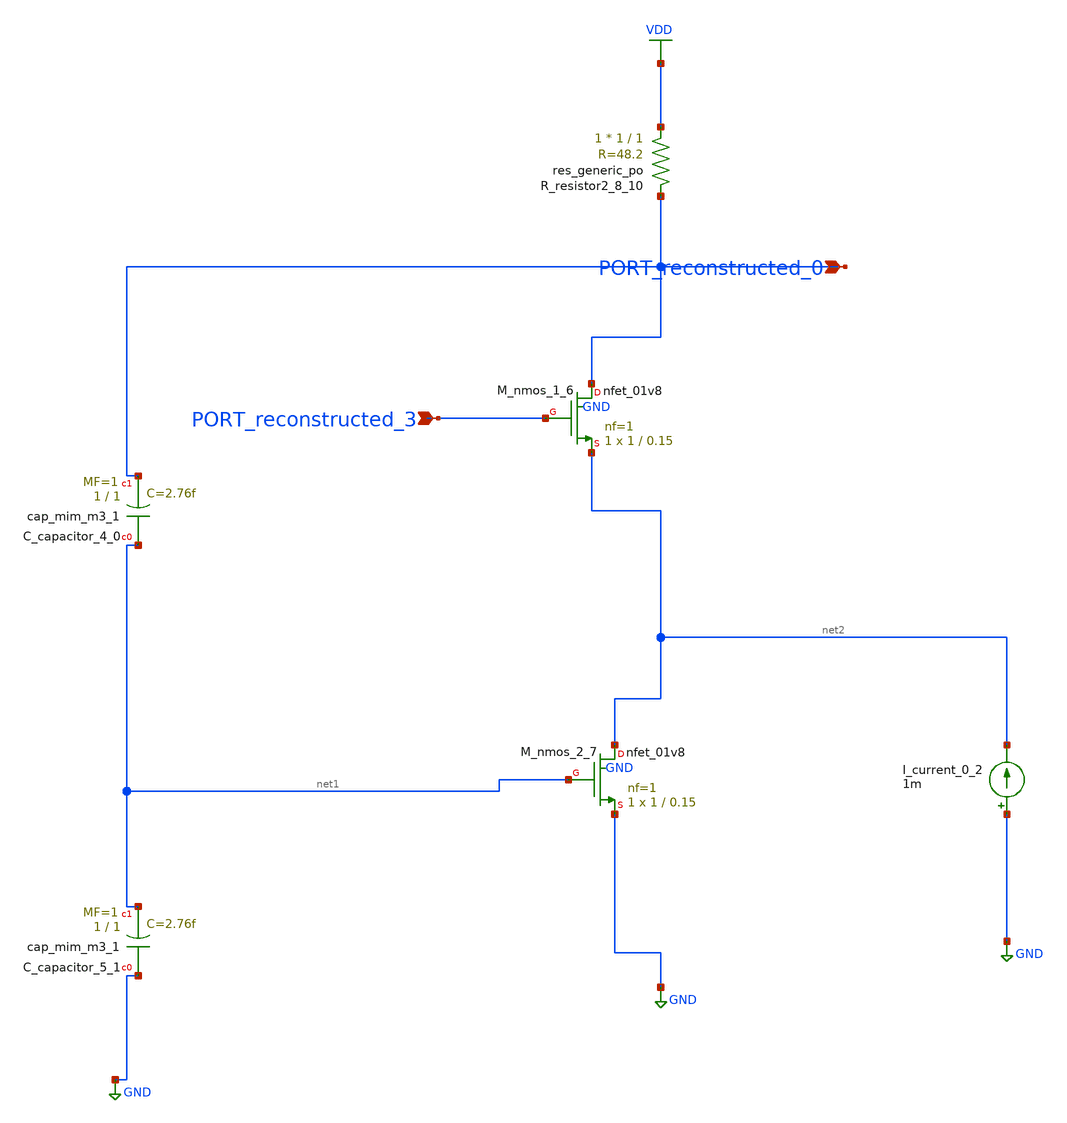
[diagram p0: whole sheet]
** sch_path: schematics/AMSNet/558.sch
**.subckt 558 PORT_reconstructed_0 PORT_reconstructed_3
*.ipin PORT_reconstructed_0
*.ipin PORT_reconstructed_3
XC_capacitor_4_0 net1 PORT_reconstructed_0 sky130_fd_pr__cap_mim_m3_1 W=1 L=1 MF=1 m=1
XC_capacitor_5_1 GND net1 sky130_fd_pr__cap_mim_m3_1 W=1 L=1 MF=1 m=1
I_current_0_2 GND net2 1m
XM_nmos_1_6 PORT_reconstructed_0 PORT_reconstructed_3 net2 GND sky130_fd_pr__nfet_01v8 L=0.15 W=1 nf=1
+ ad='int((1 + 1)/2) * 1 / 1 * 0.29' as='int((1 + 2)/2) * 1 / 1 * 0.29' pd='2*int((1 + 1)/2) * (1 / 1 + 0.29)'
+ ps='2*int((1 + 2)/2) * (1 / 1 + 0.29)' nrd='0.29 / 1 ' nrs='0.29 / 1 ' sa=0 sb=0 sd=0 mult=1 m=1
XM_nmos_2_7 net2 net1 GND GND sky130_fd_pr__nfet_01v8 L=0.15 W=1 nf=1 ad='int((1 + 1)/2) * 1 / 1 * 0.29'
+ as='int((1 + 2)/2) * 1 / 1 * 0.29' pd='2*int((1 + 1)/2) * (1 / 1 + 0.29)' ps='2*int((1 + 2)/2) * (1 / 1 + 0.29)'
+ nrd='0.29 / 1 ' nrs='0.29 / 1 ' sa=0 sb=0 sd=0 mult=1 m=1
XR_resistor2_8_10 VDD PORT_reconstructed_0 sky130_fd_pr__res_generic_po W=1 L=1 m=1
**.ends
.GLOBAL GND
.GLOBAL VDD
.end
